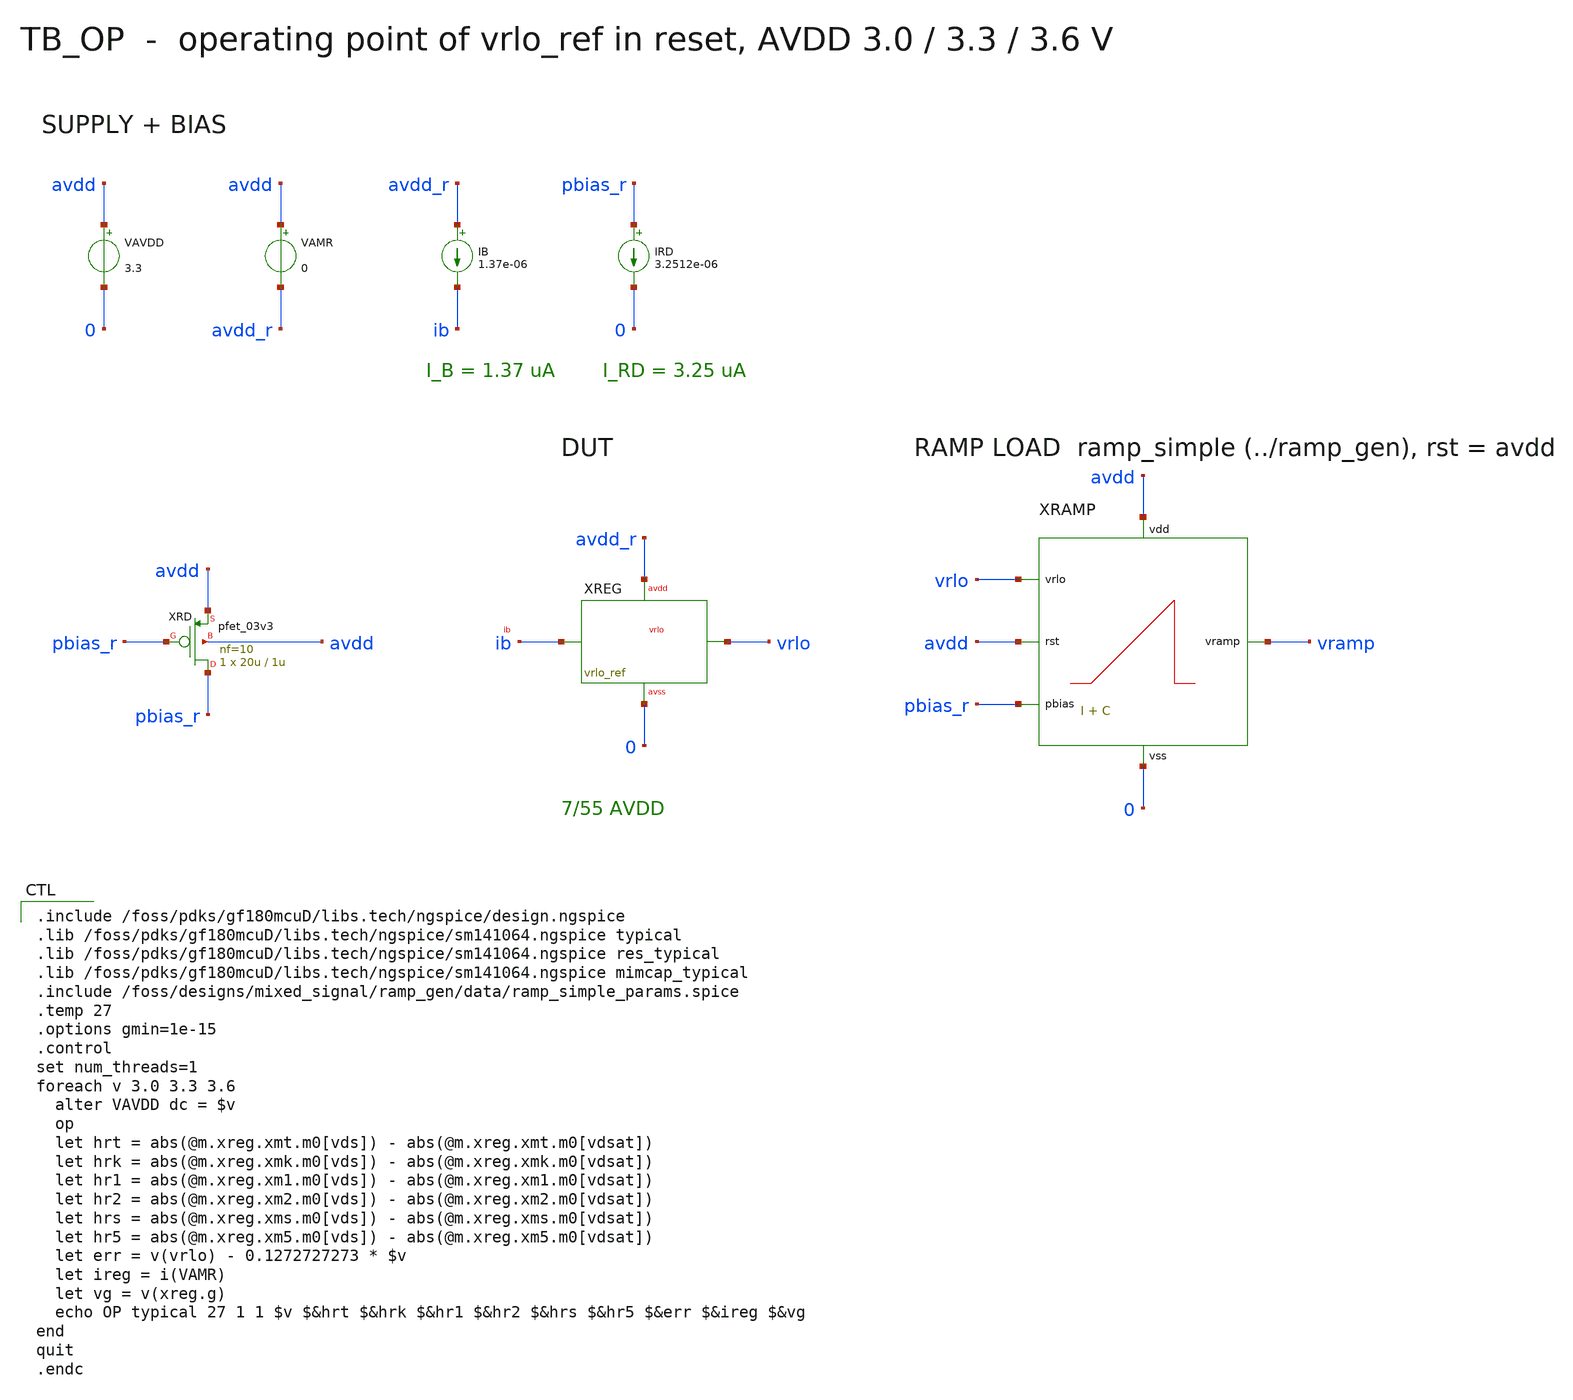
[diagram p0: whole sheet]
** sch_path: mixed_signal/vrlo_ref/tb_op.sch
**.subckt tb_op
VAVDD avdd 0 3.3
VAMR avdd avdd_r 0
IB avdd_r ib 1.37e-06
XREG vrlo ib avdd_r 0 vrlo_ref
IRD pbias_r 0 3.2512e-06
XRD pbias_r pbias_r avdd avdd pfet_03v3 L=1u W=20u nf=10 m=1
XRAMP vramp avdd vrlo pbias_r avdd 0 ramp_simple
**** begin user architecture code

.include /foss/pdks/gf180mcuD/libs.tech/ngspice/design.ngspice
.lib /foss/pdks/gf180mcuD/libs.tech/ngspice/sm141064.ngspice typical
.lib /foss/pdks/gf180mcuD/libs.tech/ngspice/sm141064.ngspice res_typical
.lib /foss/pdks/gf180mcuD/libs.tech/ngspice/sm141064.ngspice mimcap_typical
.include /foss/designs/mixed_signal/ramp_gen/data/ramp_simple_params.spice
.temp 27
.options gmin=1e-15
.control
set num_threads=1
foreach v 3.0 3.3 3.6
  alter VAVDD dc = $v
  op
  let hrt = abs(@m.xreg.xmt.m0[vds]) - abs(@m.xreg.xmt.m0[vdsat])
  let hrk = abs(@m.xreg.xmk.m0[vds]) - abs(@m.xreg.xmk.m0[vdsat])
  let hr1 = abs(@m.xreg.xm1.m0[vds]) - abs(@m.xreg.xm1.m0[vdsat])
  let hr2 = abs(@m.xreg.xm2.m0[vds]) - abs(@m.xreg.xm2.m0[vdsat])
  let hrs = abs(@m.xreg.xms.m0[vds]) - abs(@m.xreg.xms.m0[vdsat])
  let hr5 = abs(@m.xreg.xm5.m0[vds]) - abs(@m.xreg.xm5.m0[vdsat])
  let err = v(vrlo) - 0.1272727273 * $v
  let ireg = i(VAMR)
  let vg = v(xreg.g)
  echo OP typical 27 1 1 $v $&hrt $&hrk $&hr1 $&hr2 $&hrs $&hr5 $&err $&ireg $&vg
end
quit
.endc

**** end user architecture code
**.ends
.end
